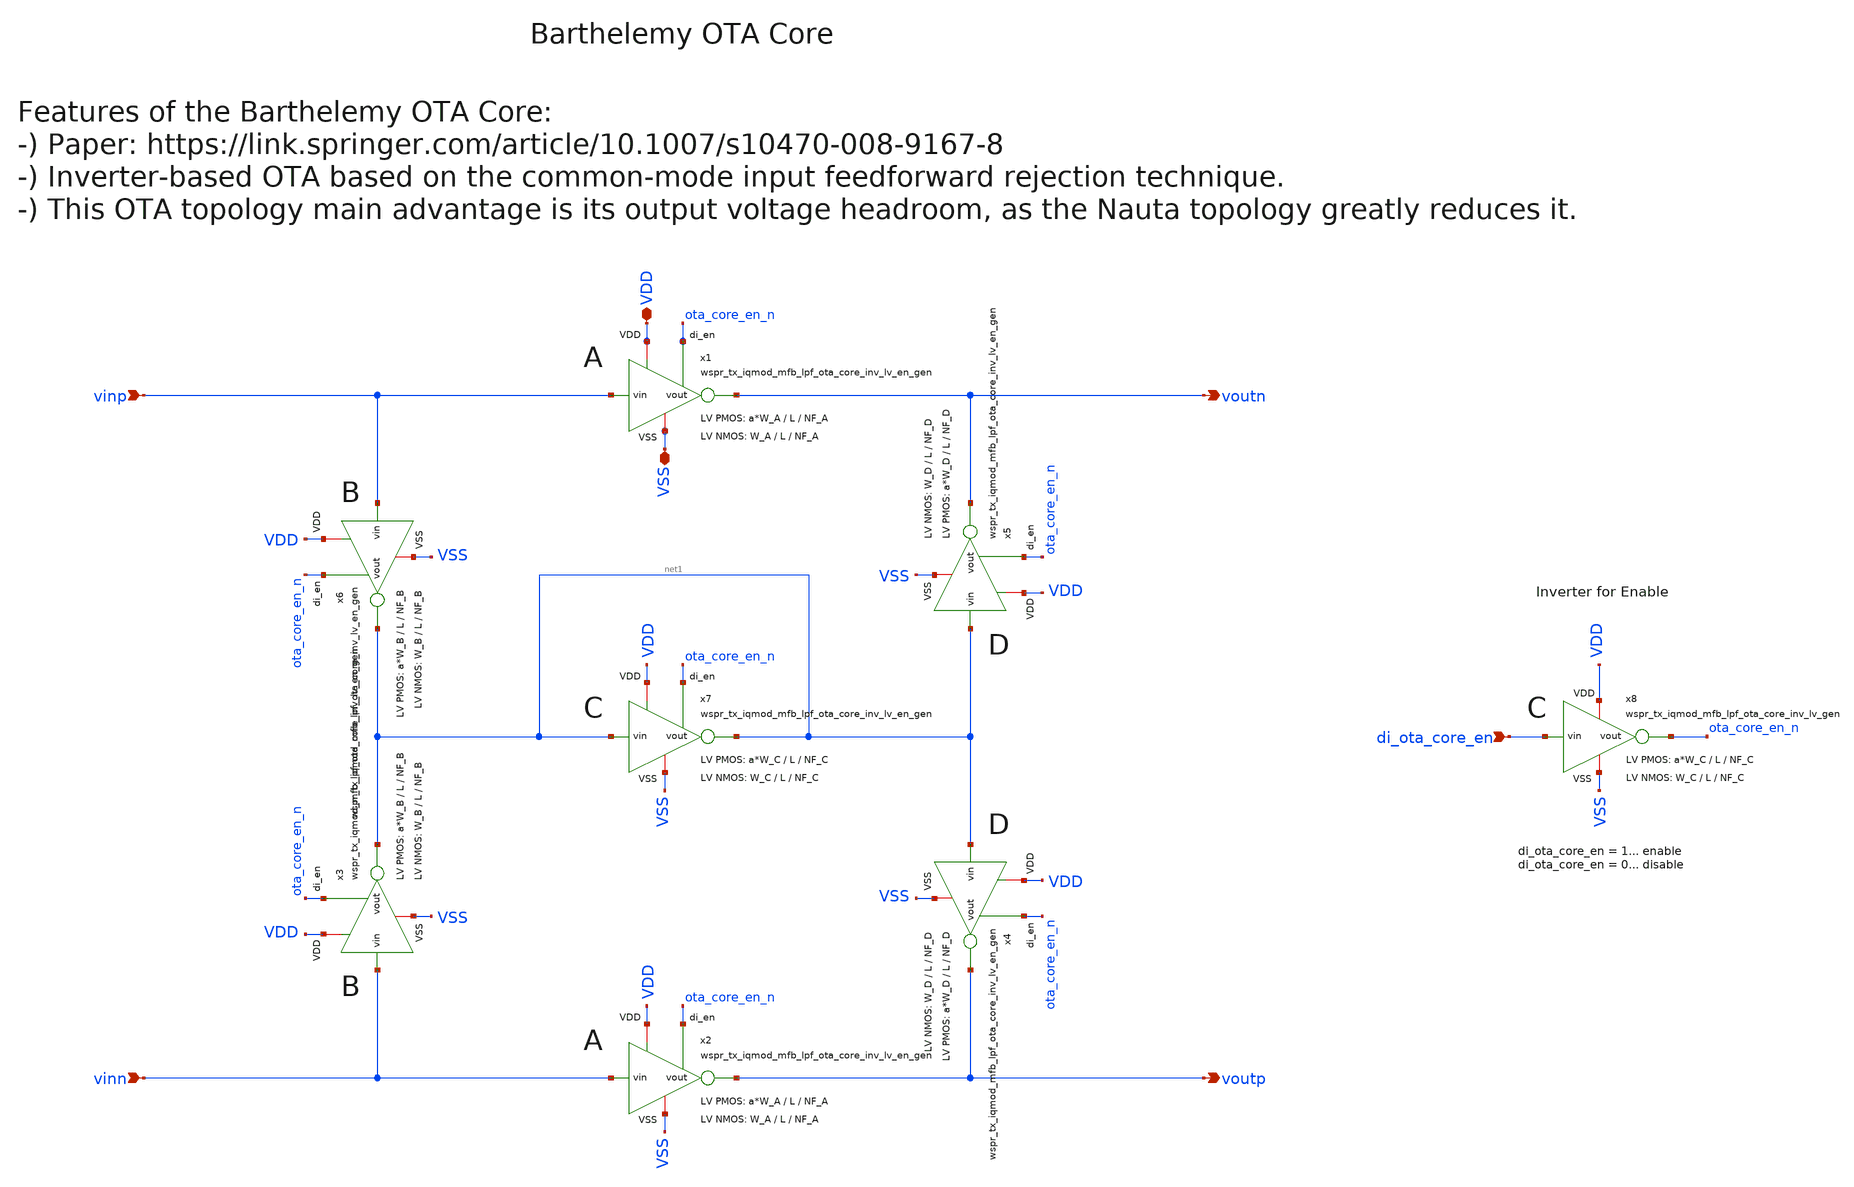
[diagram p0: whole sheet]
** sch_path: sky130/macros/iqmod/schematic/generic/wspr_tx_iqmod_mfb_lpf_ota_core_barthelemy_gen.sch
**.subckt wspr_tx_iqmod_mfb_lpf_ota_core_barthelemy_gen di_ota_core_en vinp vinn voutp voutn VDD VSS
*.ipin di_ota_core_en
*.ipin vinp
*.ipin vinn
*.opin voutp
*.opin voutn
*.iopin VDD
*.iopin VSS
x2 VDD vinn voutp VSS ota_core_en_n wspr_tx_iqmod_mfb_lpf_ota_core_inv_lv_en_gen W_P=a*W_A L_P=L
+ NF_P=NF_A W_N=W_A L_N=L NF_N=NF_A
x1 VDD vinp voutn VSS ota_core_en_n wspr_tx_iqmod_mfb_lpf_ota_core_inv_lv_en_gen W_P=a*W_A L_P=L
+ NF_P=NF_A W_N=W_A L_N=L NF_N=NF_A
x4 VDD net1 voutp VSS ota_core_en_n wspr_tx_iqmod_mfb_lpf_ota_core_inv_lv_en_gen W_P=a*W_D L_P=L
+ NF_P=NF_D W_N=W_D L_N=L NF_N=NF_D
x5 VDD net1 voutn VSS ota_core_en_n wspr_tx_iqmod_mfb_lpf_ota_core_inv_lv_en_gen W_P=a*W_D L_P=L
+ NF_P=NF_D W_N=W_D L_N=L NF_N=NF_D
x6 VDD vinp net1 VSS ota_core_en_n wspr_tx_iqmod_mfb_lpf_ota_core_inv_lv_en_gen W_P=a*W_B L_P=L
+ NF_P=NF_B W_N=W_B L_N=L NF_N=NF_B
x3 VDD vinn net1 VSS ota_core_en_n wspr_tx_iqmod_mfb_lpf_ota_core_inv_lv_en_gen W_P=a*W_B L_P=L
+ NF_P=NF_B W_N=W_B L_N=L NF_N=NF_B
x7 VDD net1 net1 VSS ota_core_en_n wspr_tx_iqmod_mfb_lpf_ota_core_inv_lv_en_gen W_P=a*W_C L_P=L
+ NF_P=NF_C W_N=W_C L_N=L NF_N=NF_C
x8 VDD di_ota_core_en ota_core_en_n VSS wspr_tx_iqmod_mfb_lpf_ota_core_inv_lv_gen W_P=a*W_C L_P=L
+ NF_P=NF_C W_N=W_C L_N=L NF_N=NF_C
**.ends
.end
